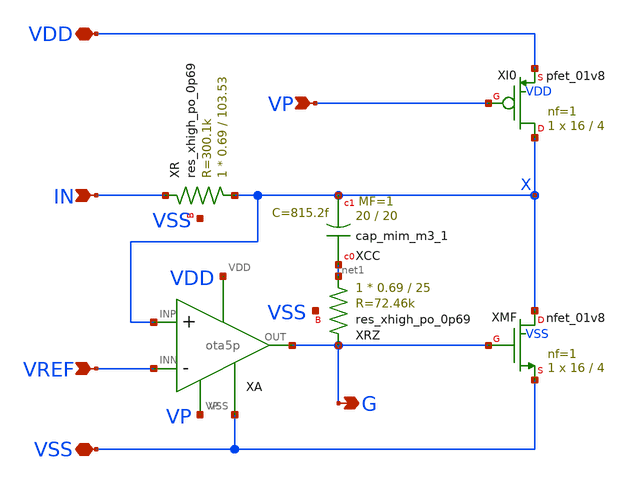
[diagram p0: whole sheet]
** sch_path: xschem/vi_conv.sch
**.subckt vi_conv IN VREF VP G VDD VSS
*.ipin IN
*.ipin VREF
*.ipin VP
*.opin G
*.iopin VDD
*.iopin VSS
XXI0 X VP VDD VDD sky130_fd_pr__pfet_01v8 L=4 W=16 nf=1 ad='int((1 + 1)/2) * 16 / 1 * 0.29' as='int((1 + 2)/2) * 16 / 1 * 0.29'
+ pd='2*int((1 + 1)/2) * (16 / 1 + 0.29)' ps='2*int((1 + 2)/2) * (16 / 1 + 0.29)' nrd='0.29 / 16 ' nrs='0.29 / 16 '
+ sa=0 sb=0 sd=0 mult=1 m=1
XXMF X G VSS VSS sky130_fd_pr__nfet_01v8 L=4 W=16 nf=1 ad='int((nf+1)/2) * W/nf * 0.29' as='int((nf+2)/2) * W/nf * 0.29'
+ pd='2*int((nf+1)/2) * (W/nf + 0.29)' ps='2*int((nf+2)/2) * (W/nf + 0.29)' nrd='0.29 / W' nrs='0.29 / W'
+ sa=0 sb=0 sd=0 mult=1 m=1
XXR X IN VSS sky130_fd_pr__res_xhigh_po_0p69 L=103.53 mult=1 m=1
XXCC net1 X sky130_fd_pr__cap_mim_m3_1 W=20 L=20 MF=1 m=1
XXRZ net1 G VSS sky130_fd_pr__res_xhigh_po_0p69 L=25 mult=1 m=1
XA X VREF G VP VDD VSS ota5p
**.ends

* expanding   symbol:  ota5p.sym # of pins=6
** sym_path: xschem/ota5p.sym
** sch_path: xschem/ota5p.sch
.subckt ota5p INP INN OUT VP VDD VSS
*.ipin INP
*.ipin INN
*.ipin VP
*.opin OUT
*.iopin VDD
*.iopin VSS
XXM1 D1 INP T T sky130_fd_pr__pfet_01v8 L=1 W=10 nf=1 ad='int((1 + 1)/2) * 10 / 1 * 0.29' as='int((1 + 2)/2) * 10 / 1 * 0.29'
+ pd='2*int((1 + 1)/2) * (10 / 1 + 0.29)' ps='2*int((1 + 2)/2) * (10 / 1 + 0.29)' nrd='0.29 / 10 ' nrs='0.29 / 10 '
+ sa=0 sb=0 sd=0 mult=1 m=1
XXM2 OUT INN T T sky130_fd_pr__pfet_01v8 L=1 W=10 nf=1 ad='int((1 + 1)/2) * 10 / 1 * 0.29' as='int((1 + 2)/2) * 10 / 1 * 0.29'
+ pd='2*int((1 + 1)/2) * (10 / 1 + 0.29)' ps='2*int((1 + 2)/2) * (10 / 1 + 0.29)' nrd='0.29 / 10 ' nrs='0.29 / 10 '
+ sa=0 sb=0 sd=0 mult=1 m=1
XXMT T VP VDD VDD sky130_fd_pr__pfet_01v8 L=2 W=16 nf=1 ad='int((1 + 1)/2) * 16 / 1 * 0.29' as='int((1 + 2)/2) * 16 / 1 * 0.29'
+ pd='2*int((1 + 1)/2) * (16 / 1 + 0.29)' ps='2*int((1 + 2)/2) * (16 / 1 + 0.29)' nrd='0.29 / 16 ' nrs='0.29 / 16 '
+ sa=0 sb=0 sd=0 mult=1 m=1
XXM3 D1 D1 VSS VSS sky130_fd_pr__nfet_01v8 L=2 W=2 nf=1 ad='int((nf+1)/2) * W/nf * 0.29' as='int((nf+2)/2) * W/nf * 0.29'
+ pd='2*int((nf+1)/2) * (W/nf + 0.29)' ps='2*int((nf+2)/2) * (W/nf + 0.29)' nrd='0.29 / W' nrs='0.29 / W'
+ sa=0 sb=0 sd=0 mult=1 m=1
XXM4 OUT D1 VSS VSS sky130_fd_pr__nfet_01v8 L=2 W=2 nf=1 ad='int((nf+1)/2) * W/nf * 0.29' as='int((nf+2)/2) * W/nf * 0.29'
+ pd='2*int((nf+1)/2) * (W/nf + 0.29)' ps='2*int((nf+2)/2) * (W/nf + 0.29)' nrd='0.29 / W' nrs='0.29 / W'
+ sa=0 sb=0 sd=0 mult=1 m=1
.ends

.end
